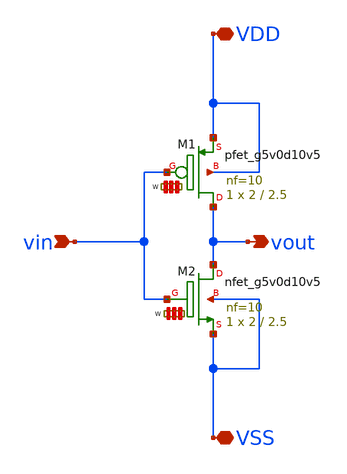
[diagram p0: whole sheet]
** sch_path: macros/inverter/schematic/xschem/inverter.sch
**.subckt inverter VDD VSS vin vout
*.iopin VDD
*.iopin VSS
*.ipin vin
*.opin vout
XM1 vout vin VDD VDD sky130_fd_pr__pfet_g5v0d10v5 L=2.5 W='2 * 10 ' nf=10 ad='int((10 + 1)/2) * 2 / 10 * 0.29'
+ as='int((10 + 2)/2) * 2 / 10 * 0.29' pd='2*int((10 + 1)/2) * (2 / 10 + 0.29)' ps='2*int((10 + 2)/2) * (2 / 10 + 0.29)'
+ nrd='0.29 / 2 ' nrs='0.29 / 2 ' sa=0 sb=0 sd=0 mult=1 m=1
XM2 vout vin VSS VSS sky130_fd_pr__nfet_g5v0d10v5 L=2.5 W='2 * 10 ' nf=10 ad='int((10 + 1)/2) * 2 / 10 * 0.29'
+ as='int((10 + 2)/2) * 2 / 10 * 0.29' pd='2*int((10 + 1)/2) * (2 / 10 + 0.29)' ps='2*int((10 + 2)/2) * (2 / 10 + 0.29)'
+ nrd='0.29 / 2 ' nrs='0.29 / 2 ' sa=0 sb=0 sd=0 mult=1 m=1
**.ends
.end
